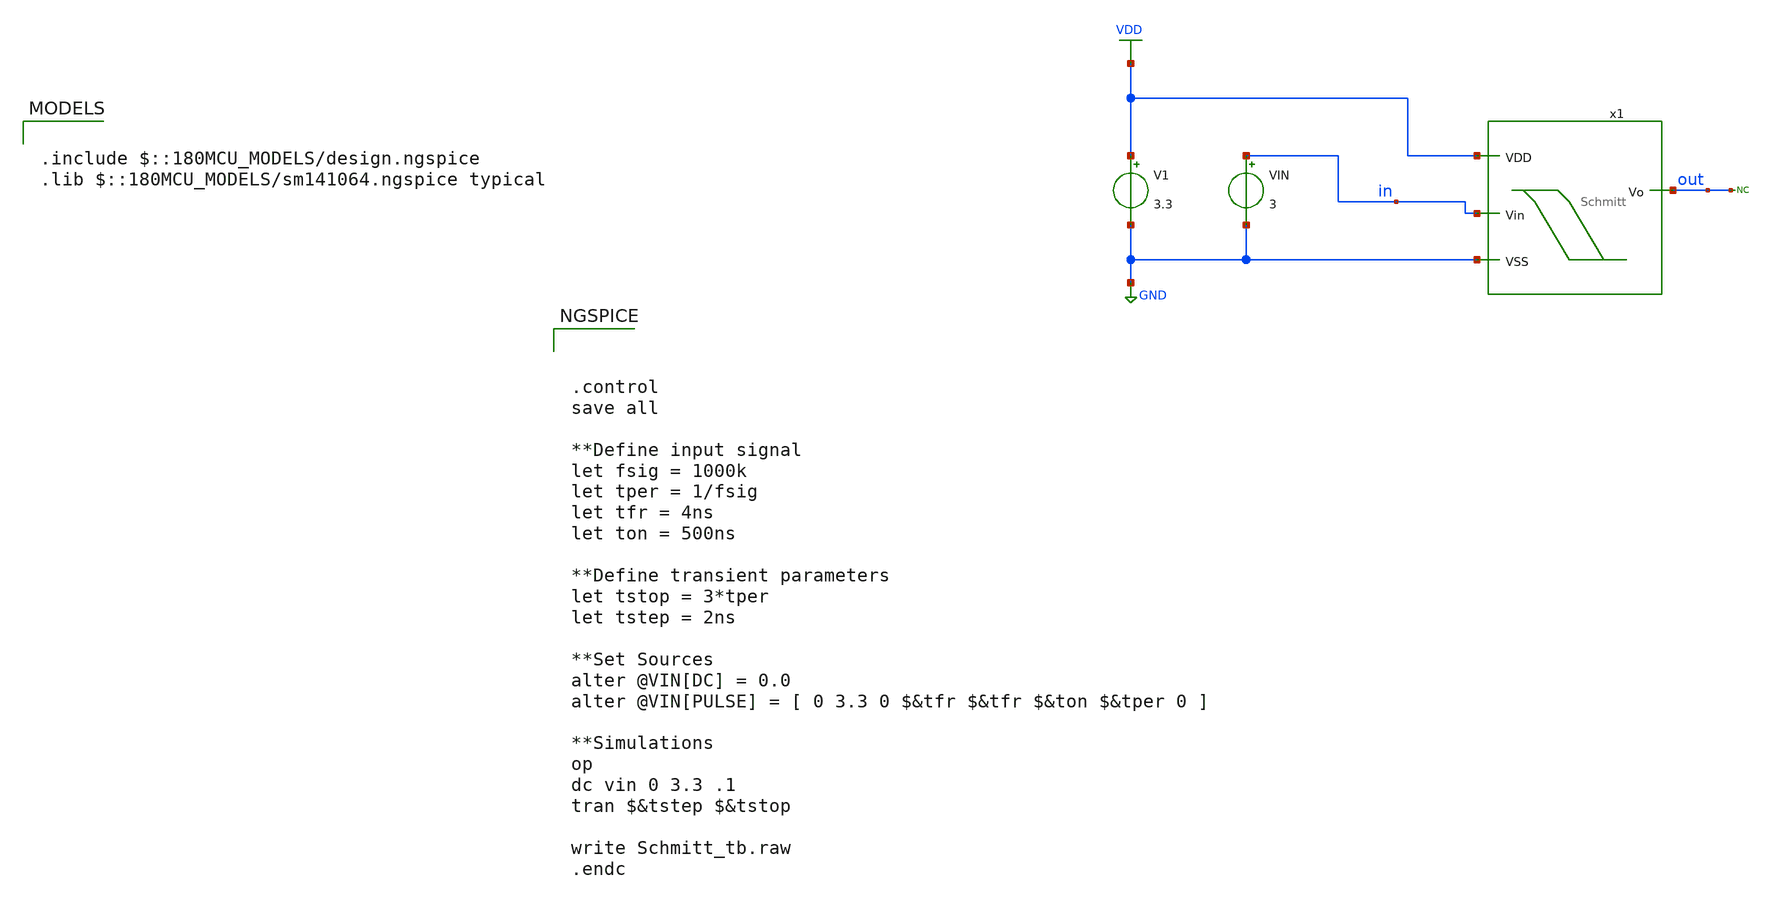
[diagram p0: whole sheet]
** sch_path: designs/Schmitt_tb.sch
**.subckt Schmitt_tb
x1 VDD in out GND Schmitt
V1 VDD GND 3.3
VIN in GND 3
* noconn out
**** begin user architecture code



.control
save all

**Define input signal
let fsig = 1000k
let tper = 1/fsig
let tfr = 4ns
let ton = 500ns

**Define transient parameters
let tstop = 3*tper
let tstep = 2ns

**Set Sources
alter @VIN[DC] = 0.0
alter @VIN[PULSE] = [ 0 3.3 0 $&tfr $&tfr $&ton $&tper 0 ]

**Simulations
op
dc vin 0 3.3 .1
tran $&tstep $&tstop

write Schmitt_tb.raw
.endc



.include $::180MCU_MODELS/design.ngspice
.lib $::180MCU_MODELS/sm141064.ngspice typical

**** end user architecture code
**.ends

* expanding   symbol:  Schmitt.sym # of pins=4
** sym_path: Schmitt.sym
** sch_path: Schmitt.sch
.subckt Schmitt VDD Vin Vo VSS
*.ipin VDD
*.ipin VSS
*.ipin Vin
*.opin Vo
XM1 Vo Vin net2 VSS nfet_03v3 L=0.28u W=0.22u nf=1 ad='int((nf+1)/2) * W/nf * 0.18u' as='int((nf+2)/2) * W/nf * 0.18u'
+ pd='2*int((nf+1)/2) * (W/nf + 0.18u)' ps='2*int((nf+2)/2) * (W/nf + 0.18u)' nrd='0.18u / W' nrs='0.18u / W'
+ sa=0 sb=0 sd=0 m=1
XM2 net1 Vin VDD VDD pfet_03v3 L=0.28u W=0.22u nf=1 ad='int((nf+1)/2) * W/nf * 0.18u' as='int((nf+2)/2) * W/nf * 0.18u'
+ pd='2*int((nf+1)/2) * (W/nf + 0.18u)' ps='2*int((nf+2)/2) * (W/nf + 0.18u)' nrd='0.18u / W' nrs='0.18u / W'
+ sa=0 sb=0 sd=0 m=1
XM3 Vo Vin net1 VDD pfet_03v3 L=0.28u W=0.22u nf=1 ad='int((nf+1)/2) * W/nf * 0.18u' as='int((nf+2)/2) * W/nf * 0.18u'
+ pd='2*int((nf+1)/2) * (W/nf + 0.18u)' ps='2*int((nf+2)/2) * (W/nf + 0.18u)' nrd='0.18u / W' nrs='0.18u / W'
+ sa=0 sb=0 sd=0 m=1
XM4 net2 Vin VSS VSS nfet_03v3 L=0.28u W=0.22u nf=1 ad='int((nf+1)/2) * W/nf * 0.18u' as='int((nf+2)/2) * W/nf * 0.18u'
+ pd='2*int((nf+1)/2) * (W/nf + 0.18u)' ps='2*int((nf+2)/2) * (W/nf + 0.18u)' nrd='0.18u / W' nrs='0.18u / W'
+ sa=0 sb=0 sd=0 m=1
XM5 VDD Vo net2 VSS nfet_03v3 L=0.28u W=0.22u nf=1 ad='int((nf+1)/2) * W/nf * 0.18u' as='int((nf+2)/2) * W/nf * 0.18u'
+ pd='2*int((nf+1)/2) * (W/nf + 0.18u)' ps='2*int((nf+2)/2) * (W/nf + 0.18u)' nrd='0.18u / W' nrs='0.18u / W'
+ sa=0 sb=0 sd=0 m=1
XM6 VSS Vo net1 VDD pfet_03v3 L=0.28u W=0.22u nf=1 ad='int((nf+1)/2) * W/nf * 0.18u' as='int((nf+2)/2) * W/nf * 0.18u'
+ pd='2*int((nf+1)/2) * (W/nf + 0.18u)' ps='2*int((nf+2)/2) * (W/nf + 0.18u)' nrd='0.18u / W' nrs='0.18u / W'
+ sa=0 sb=0 sd=0 m=1
.ends

.GLOBAL GND
.GLOBAL VDD
.end
